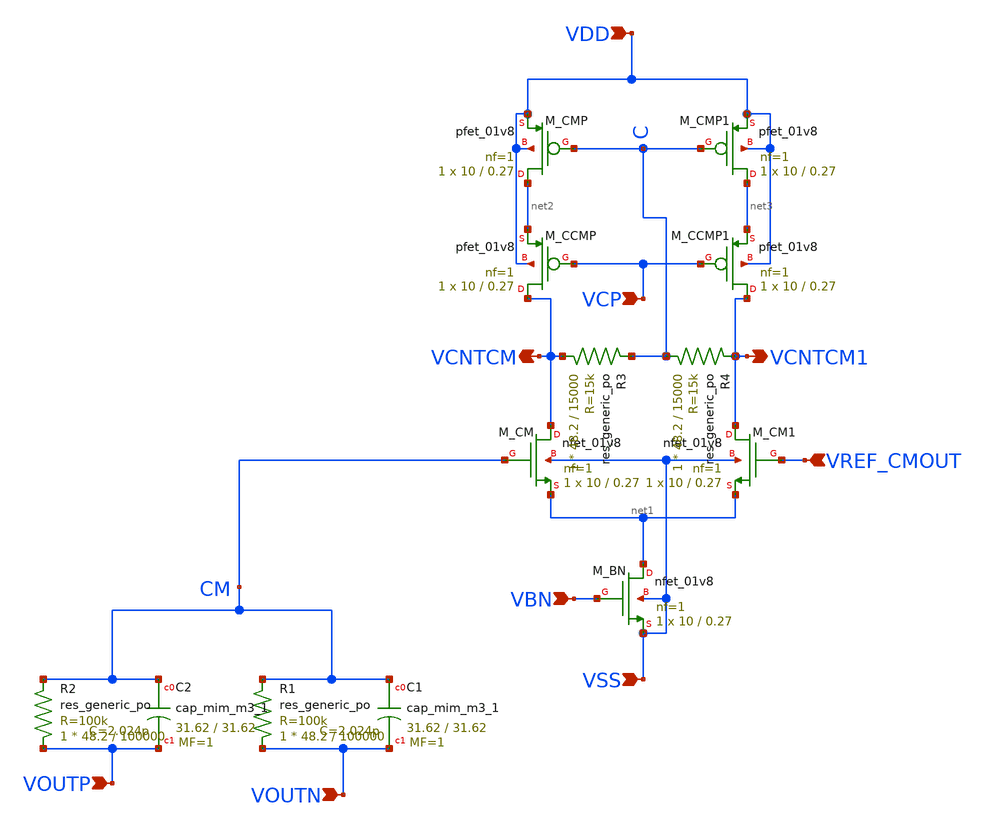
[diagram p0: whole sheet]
** sch_path: cmfb.sch
**.subckt cmfb VDD VSS VOUTP VOUTN VBN VCP VREF_CMOUT VCNTCM VCNTCM1
*.ipin VDD
*.ipin VSS
*.ipin VOUTP
*.ipin VOUTN
*.ipin VBN
*.ipin VCP
*.ipin VREF_CMOUT
*.opin VCNTCM
*.opin VCNTCM1
XR1 VOUTN CM sky130_fd_pr__res_generic_po W=48.2 L=100000 m=1
XR2 VOUTP CM sky130_fd_pr__res_generic_po W=48.2 L=100000 m=1
XC1 CM VOUTN sky130_fd_pr__cap_mim_m3_1 W=31.62 L=31.62 MF=1 m=1
XC2 CM VOUTP sky130_fd_pr__cap_mim_m3_1 W=31.62 L=31.62 MF=1 m=1
XM_CM VCNTCM CM net1 VSS sky130_fd_pr__nfet_01v8 L=0.27 W=10 nf=1 ad='int((1 + 1)/2) * 10 / 1 * 0.29'
+ as='int((1 + 2)/2) * 10 / 1 * 0.29' pd='2*int((1 + 1)/2) * (10 / 1 + 0.29)' ps='2*int((1 + 2)/2) * (10 / 1 + 0.29)'
+ nrd='0.29 / 10 ' nrs='0.29 / 10 ' sa=0 sb=0 sd=0 mult=1 m=1
XM_CM1 VCNTCM1 VREF_CMOUT net1 VSS sky130_fd_pr__nfet_01v8 L=0.27 W=10 nf=1 ad='int((1 + 1)/2) * 10 / 1 * 0.29'
+ as='int((1 + 2)/2) * 10 / 1 * 0.29' pd='2*int((1 + 1)/2) * (10 / 1 + 0.29)' ps='2*int((1 + 2)/2) * (10 / 1 + 0.29)'
+ nrd='0.29 / 10 ' nrs='0.29 / 10 ' sa=0 sb=0 sd=0 mult=1 m=1
XM_BN net1 VBN VSS VSS sky130_fd_pr__nfet_01v8 L=0.27 W=10 nf=1 ad='int((1 + 1)/2) * 10 / 1 * 0.29' as='int((1 + 2)/2) * 10 / 1 * 0.29'
+ pd='2*int((1 + 1)/2) * (10 / 1 + 0.29)' ps='2*int((1 + 2)/2) * (10 / 1 + 0.29)' nrd='0.29 / 10 ' nrs='0.29 / 10 '
+ sa=0 sb=0 sd=0 mult=1 m=1
XM_CMP net2 C VDD VDD sky130_fd_pr__pfet_01v8 L=0.27 W=10 nf=1 ad='int((1 + 1)/2) * 10 / 1 * 0.29' as='int((1 + 2)/2) * 10 / 1 * 0.29'
+ pd='2*int((1 + 1)/2) * (10 / 1 + 0.29)' ps='2*int((1 + 2)/2) * (10 / 1 + 0.29)' nrd='0.29 / 10 ' nrs='0.29 / 10 '
+ sa=0 sb=0 sd=0 mult=1 m=1
XM_CMP1 net3 C VDD VDD sky130_fd_pr__pfet_01v8 L=0.27 W=10 nf=1 ad='int((1 + 1)/2) * 10 / 1 * 0.29' as='int((1 + 2)/2) * 10 / 1 * 0.29'
+ pd='2*int((1 + 1)/2) * (10 / 1 + 0.29)' ps='2*int((1 + 2)/2) * (10 / 1 + 0.29)' nrd='0.29 / 10 ' nrs='0.29 / 10 '
+ sa=0 sb=0 sd=0 mult=1 m=1
XM_CCMP VCNTCM VCP net2 VDD sky130_fd_pr__pfet_01v8 L=0.27 W=10 nf=1 ad='int((1 + 1)/2) * 10 / 1 * 0.29'
+ as='int((1 + 2)/2) * 10 / 1 * 0.29' pd='2*int((1 + 1)/2) * (10 / 1 + 0.29)' ps='2*int((1 + 2)/2) * (10 / 1 + 0.29)'
+ nrd='0.29 / 10 ' nrs='0.29 / 10 ' sa=0 sb=0 sd=0 mult=1 m=1
XM_CCMP1 VCNTCM1 VCP net3 VDD sky130_fd_pr__pfet_01v8 L=0.27 W=10 nf=1 ad='int((1 + 1)/2) * 10 / 1 * 0.29'
+ as='int((1 + 2)/2) * 10 / 1 * 0.29' pd='2*int((1 + 1)/2) * (10 / 1 + 0.29)' ps='2*int((1 + 2)/2) * (10 / 1 + 0.29)'
+ nrd='0.29 / 10 ' nrs='0.29 / 10 ' sa=0 sb=0 sd=0 mult=1 m=1
XR3 VCNTCM C sky130_fd_pr__res_generic_po W=48.2 L=15000 m=1
XR4 C VCNTCM1 sky130_fd_pr__res_generic_po W=48.2 L=15000 m=1
**.ends
.end
